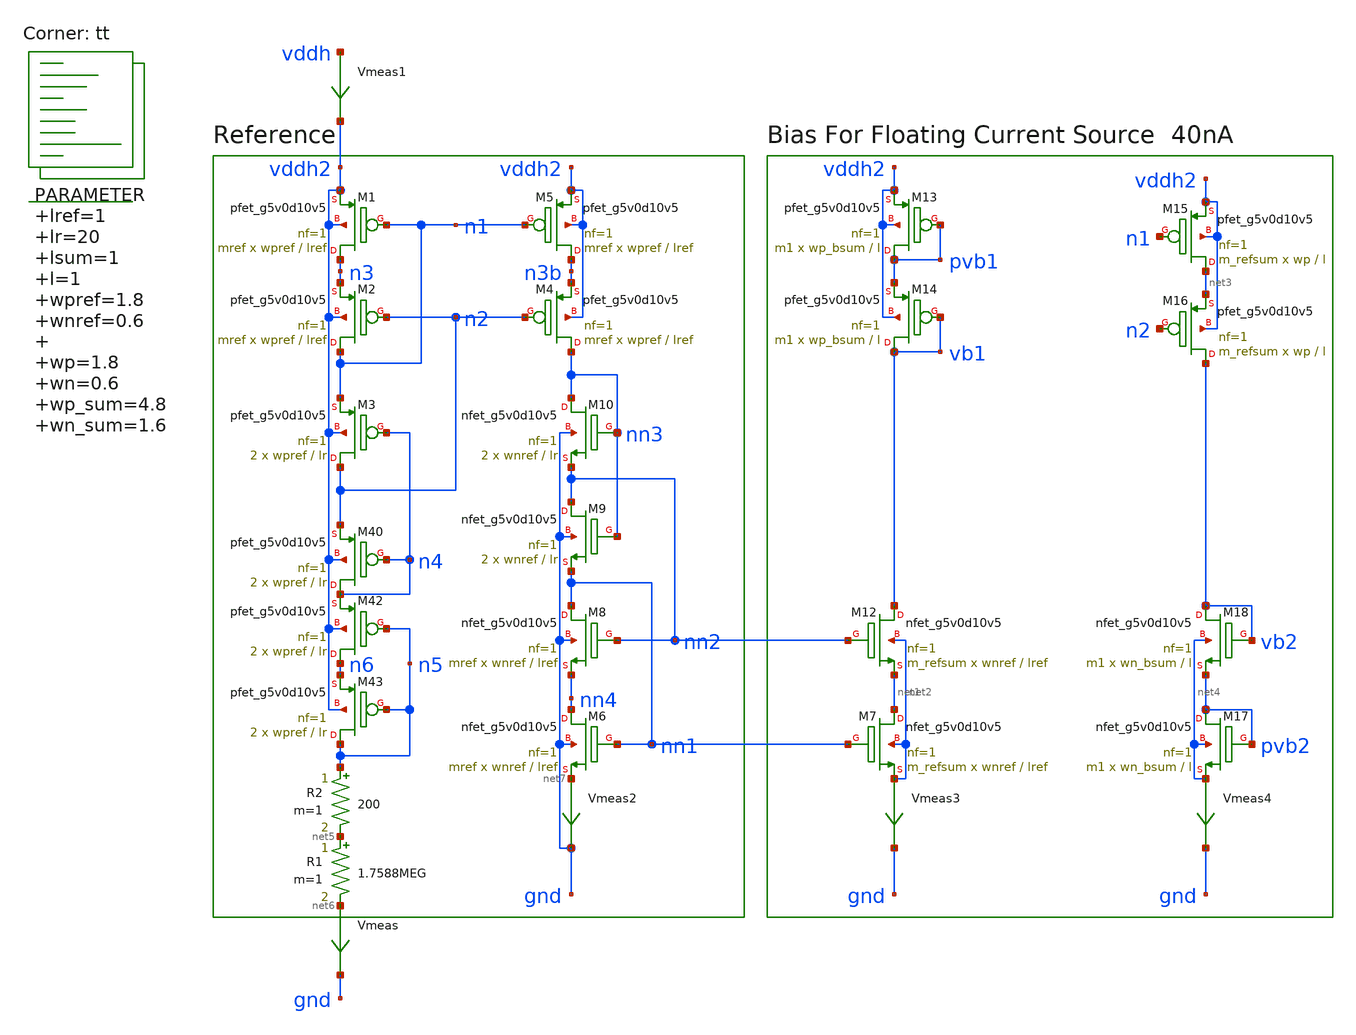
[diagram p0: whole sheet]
** sch_path: xschem/op_amp_biasing.sch
**.subckt op_amp_biasing
.param lref=1 lr=20 lsum=1 l=1 wpref=1.8 wnref=0.6 wp=1.8 wn=0.6 wp_sum=4.8 wn_sum=1.6 wp_fcm=4.8
+ wn_fcm=1.6 wp_head=3 wn_tail=1 wp_bsum=4.8 wn_bsum=1.6 mref=20 m1=2 m_sum=2 m_refsum=8 m_fcm=2 mdiff0=2 m=1
XM1 n3 n1 vddh2 vddh2 sky130_fd_pr__pfet_g5v0d10v5 L=lref W=wpref nf=1 ad='int((nf+1)/2) * W/nf * 0.29'
+ as='int((nf+2)/2) * W/nf * 0.29' pd='2*int((nf+1)/2) * (W/nf + 0.29)' ps='2*int((nf+2)/2) * (W/nf + 0.29)'
+ nrd='0.29 / W' nrs='0.29 / W' sa=0 sb=0 sd=0 mult=mref m=mref
R1 net5 net6 1.7588MEG m=1
Vmeas net6 gnd 0
.save i(vmeas)
R2 n5 net5 200 m=1
Vmeas1 vddh vddh2 0
.save i(vmeas1)
XM2 n1 n2 n3 vddh2 sky130_fd_pr__pfet_g5v0d10v5 L=lref W=wpref nf=1 ad='int((nf+1)/2) * W/nf * 0.29'
+ as='int((nf+2)/2) * W/nf * 0.29' pd='2*int((nf+1)/2) * (W/nf + 0.29)' ps='2*int((nf+2)/2) * (W/nf + 0.29)'
+ nrd='0.29 / W' nrs='0.29 / W' sa=0 sb=0 sd=0 mult=mref m=mref
XM3 n2 n4 n1 vddh2 sky130_fd_pr__pfet_g5v0d10v5 L=lr W=wpref nf=1 ad='int((nf+1)/2) * W/nf * 0.29' as='int((nf+2)/2) * W/nf * 0.29'
+ pd='2*int((nf+1)/2) * (W/nf + 0.29)' ps='2*int((nf+2)/2) * (W/nf + 0.29)' nrd='0.29 / W' nrs='0.29 / W'
+ sa=0 sb=0 sd=0 mult=2 m=2
XM40 n4 n4 n2 vddh2 sky130_fd_pr__pfet_g5v0d10v5 L=lr W=wpref nf=1 ad='int((nf+1)/2) * W/nf * 0.29' as='int((nf+2)/2) * W/nf * 0.29'
+ pd='2*int((nf+1)/2) * (W/nf + 0.29)' ps='2*int((nf+2)/2) * (W/nf + 0.29)' nrd='0.29 / W' nrs='0.29 / W'
+ sa=0 sb=0 sd=0 mult=2 m=2
XM42 n6 n5 n4 vddh2 sky130_fd_pr__pfet_g5v0d10v5 L=lr W=wpref nf=1 ad='int((nf+1)/2) * W/nf * 0.29' as='int((nf+2)/2) * W/nf * 0.29'
+ pd='2*int((nf+1)/2) * (W/nf + 0.29)' ps='2*int((nf+2)/2) * (W/nf + 0.29)' nrd='0.29 / W' nrs='0.29 / W'
+ sa=0 sb=0 sd=0 mult=2 m=2
XM43 n5 n5 n6 vddh2 sky130_fd_pr__pfet_g5v0d10v5 L=lr W=wpref nf=1 ad='int((nf+1)/2) * W/nf * 0.29' as='int((nf+2)/2) * W/nf * 0.29'
+ pd='2*int((nf+1)/2) * (W/nf + 0.29)' ps='2*int((nf+2)/2) * (W/nf + 0.29)' nrd='0.29 / W' nrs='0.29 / W'
+ sa=0 sb=0 sd=0 mult=2 m=2
XM8 nn1 nn2 nn4 gnd sky130_fd_pr__nfet_g5v0d10v5 L=lref W=wnref nf=1 ad='int((nf+1)/2) * W/nf * 0.29'
+ as='int((nf+2)/2) * W/nf * 0.29' pd='2*int((nf+1)/2) * (W/nf + 0.29)' ps='2*int((nf+2)/2) * (W/nf + 0.29)'
+ nrd='0.29 / W' nrs='0.29 / W' sa=0 sb=0 sd=0 mult=mref m=mref
XM9 nn2 nn3 nn1 gnd sky130_fd_pr__nfet_g5v0d10v5 L=lr W=wnref nf=1 ad='int((nf+1)/2) * W/nf * 0.29' as='int((nf+2)/2) * W/nf * 0.29'
+ pd='2*int((nf+1)/2) * (W/nf + 0.29)' ps='2*int((nf+2)/2) * (W/nf + 0.29)' nrd='0.29 / W' nrs='0.29 / W'
+ sa=0 sb=0 sd=0 mult=2 m=2
XM10 nn3 nn3 nn2 gnd sky130_fd_pr__nfet_g5v0d10v5 L=lr W=wnref nf=1 ad='int((nf+1)/2) * W/nf * 0.29'
+ as='int((nf+2)/2) * W/nf * 0.29' pd='2*int((nf+1)/2) * (W/nf + 0.29)' ps='2*int((nf+2)/2) * (W/nf + 0.29)'
+ nrd='0.29 / W' nrs='0.29 / W' sa=0 sb=0 sd=0 mult=2 m=2
Vmeas2 net7 gnd 0
.save i(vmeas2)
XM5 n3b n1 vddh2 vddh2 sky130_fd_pr__pfet_g5v0d10v5 L=lref W=wpref nf=1 ad='int((nf+1)/2) * W/nf * 0.29'
+ as='int((nf+2)/2) * W/nf * 0.29' pd='2*int((nf+1)/2) * (W/nf + 0.29)' ps='2*int((nf+2)/2) * (W/nf + 0.29)'
+ nrd='0.29 / W' nrs='0.29 / W' sa=0 sb=0 sd=0 mult=mref m=mref
XM4 nn3 n2 n3b vddh2 sky130_fd_pr__pfet_g5v0d10v5 L=lref W=wpref nf=1 ad='int((nf+1)/2) * W/nf * 0.29'
+ as='int((nf+2)/2) * W/nf * 0.29' pd='2*int((nf+1)/2) * (W/nf + 0.29)' ps='2*int((nf+2)/2) * (W/nf + 0.29)'
+ nrd='0.29 / W' nrs='0.29 / W' sa=0 sb=0 sd=0 mult=mref m=mref
XM6 nn4 nn1 net7 gnd sky130_fd_pr__nfet_g5v0d10v5 L=lref W=wnref nf=1 ad='int((nf+1)/2) * W/nf * 0.29'
+ as='int((nf+2)/2) * W/nf * 0.29' pd='2*int((nf+1)/2) * (W/nf + 0.29)' ps='2*int((nf+2)/2) * (W/nf + 0.29)'
+ nrd='0.29 / W' nrs='0.29 / W' sa=0 sb=0 sd=0 mult=mref m=mref
Vmeas3 net2 gnd 0
.save i(vmeas3)
XM17 pvb2 pvb2 net4 net4 sky130_fd_pr__nfet_g5v0d10v5 L=l W=wn_bsum nf=1 ad='int((nf+1)/2) * W/nf * 0.29'
+ as='int((nf+2)/2) * W/nf * 0.29' pd='2*int((nf+1)/2) * (W/nf + 0.29)' ps='2*int((nf+2)/2) * (W/nf + 0.29)'
+ nrd='0.29 / W' nrs='0.29 / W' sa=0 sb=0 sd=0 mult=m1 m=m1
XM18 vb2 vb2 pvb2 net4 sky130_fd_pr__nfet_g5v0d10v5 L=l W=wn_bsum nf=1 ad='int((nf+1)/2) * W/nf * 0.29'
+ as='int((nf+2)/2) * W/nf * 0.29' pd='2*int((nf+1)/2) * (W/nf + 0.29)' ps='2*int((nf+2)/2) * (W/nf + 0.29)'
+ nrd='0.29 / W' nrs='0.29 / W' sa=0 sb=0 sd=0 mult=m1 m=m1
Vmeas4 net4 gnd 0
.save i(vmeas4)
XM13 pvb1 pvb1 vddh2 vddh2 sky130_fd_pr__pfet_g5v0d10v5 L=l W=wp_bsum nf=1 ad='int((nf+1)/2) * W/nf * 0.29'
+ as='int((nf+2)/2) * W/nf * 0.29' pd='2*int((nf+1)/2) * (W/nf + 0.29)' ps='2*int((nf+2)/2) * (W/nf + 0.29)'
+ nrd='0.29 / W' nrs='0.29 / W' sa=0 sb=0 sd=0 mult=m1 m=m1
XM14 vb1 vb1 pvb1 vddh2 sky130_fd_pr__pfet_g5v0d10v5 L=l W=wp_bsum nf=1 ad='int((nf+1)/2) * W/nf * 0.29'
+ as='int((nf+2)/2) * W/nf * 0.29' pd='2*int((nf+1)/2) * (W/nf + 0.29)' ps='2*int((nf+2)/2) * (W/nf + 0.29)'
+ nrd='0.29 / W' nrs='0.29 / W' sa=0 sb=0 sd=0 mult=m1 m=m1
XM15 net3 n1 vddh2 vddh2 sky130_fd_pr__pfet_g5v0d10v5 L=l W=wp nf=1 ad='int((nf+1)/2) * W/nf * 0.29'
+ as='int((nf+2)/2) * W/nf * 0.29' pd='2*int((nf+1)/2) * (W/nf + 0.29)' ps='2*int((nf+2)/2) * (W/nf + 0.29)'
+ nrd='0.29 / W' nrs='0.29 / W' sa=0 sb=0 sd=0 mult=m_refsum m=m_refsum
XM12 vb1 nn2 net1 net2 sky130_fd_pr__nfet_g5v0d10v5 L=lref W=wnref nf=1 ad='int((nf+1)/2) * W/nf * 0.29'
+ as='int((nf+2)/2) * W/nf * 0.29' pd='2*int((nf+1)/2) * (W/nf + 0.29)' ps='2*int((nf+2)/2) * (W/nf + 0.29)'
+ nrd='0.29 / W' nrs='0.29 / W' sa=0 sb=0 sd=0 mult=m_refsum m=m_refsum
XM16 vb2 n2 net3 vddh2 sky130_fd_pr__pfet_g5v0d10v5 L=l W=wp nf=1 ad='int((nf+1)/2) * W/nf * 0.29' as='int((nf+2)/2) * W/nf * 0.29'
+ pd='2*int((nf+1)/2) * (W/nf + 0.29)' ps='2*int((nf+2)/2) * (W/nf + 0.29)' nrd='0.29 / W' nrs='0.29 / W'
+ sa=0 sb=0 sd=0 mult=m_refsum m=m_refsum
XM7 net1 nn1 net2 net2 sky130_fd_pr__nfet_g5v0d10v5 L=lref W=wnref nf=1 ad='int((nf+1)/2) * W/nf * 0.29'
+ as='int((nf+2)/2) * W/nf * 0.29' pd='2*int((nf+1)/2) * (W/nf + 0.29)' ps='2*int((nf+2)/2) * (W/nf + 0.29)'
+ nrd='0.29 / W' nrs='0.29 / W' sa=0 sb=0 sd=0 mult=m_refsum m=m_refsum
**** begin user architecture code
.lib $::SKYWATER_MODELS/sky130.lib.spice tt



  .option wnflag=1
  .option safecurrents
  ********************Static Current Sources***************************
  .param iref=10u
  *Iref n4 gnd 100n
  ********************Static Voltage Sources***************************
  Vddh vddh gnd dc 5.5
  ********************Simulation Commands*****************************
  .control
     reset
     save all
     *tran 1n 10u
     dc R1 500k 2meg 1k
     write biasing-tb.raw
     set appendwrite
*    quit 0
  .endc



**** end user architecture code
**.ends
.end
